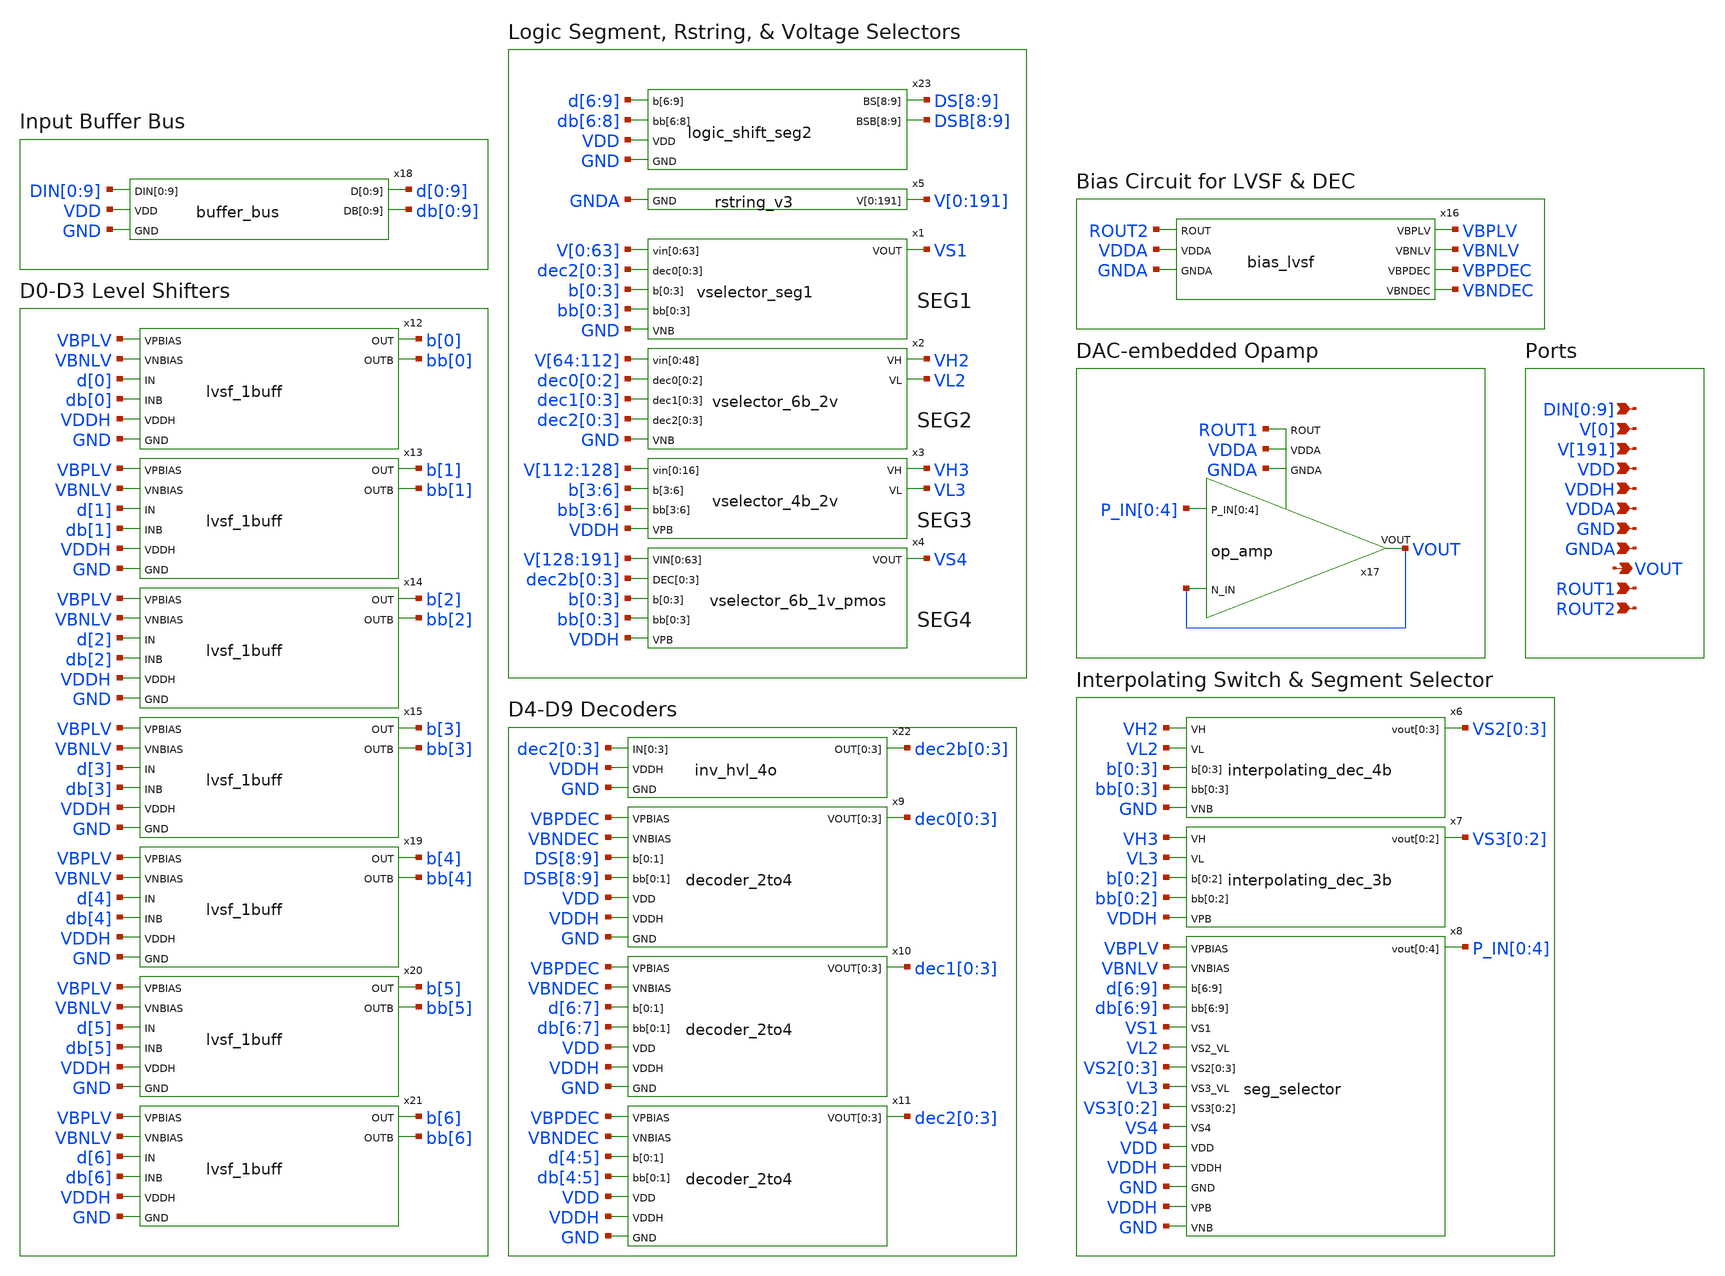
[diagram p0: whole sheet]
** sch_path: xschem/10b_DAC_top.sch
**.subckt 10b_DAC_top VOUT GND DIN[0],DIN[1],DIN[2],DIN[3],DIN[4],DIN[5],DIN[6],DIN[7],DIN[8],DIN[9]
*+ VDD VDDH VDDA GNDA ROUT1 ROUT2 V[0] V[191]
*.opin VOUT
*.ipin GND
*.ipin DIN[0],DIN[1],DIN[2],DIN[3],DIN[4],DIN[5],DIN[6],DIN[7],DIN[8],DIN[9]
*.ipin VDD
*.ipin VDDH
*.ipin VDDA
*.ipin GNDA
*.ipin ROUT1
*.ipin ROUT2
*.ipin V[0]
*.ipin V[191]
x2 V[64] V[65] V[66] V[67] V[68] V[69] V[70] V[71] V[72] V[73] V[74] V[75] V[76] V[77] V[78] V[79]
+ V[80] V[81] V[82] V[83] V[84] V[85] V[86] V[87] V[88] V[89] V[90] V[91] V[92] V[93] V[94] V[95] V[96]
+ V[97] V[98] V[99] V[100] V[101] V[102] V[103] V[104] V[105] V[106] V[107] V[108] V[109] V[110] V[111]
+ V[112] dec0[0] dec0[1] dec0[2] dec1[0] dec1[1] dec1[2] dec1[3] dec2[0] dec2[1] dec2[2] dec2[3] VH2 VL2 GND
+ vselector_6b_2v
x3 V[112] V[113] V[114] V[115] V[116] V[117] V[118] V[119] V[120] V[121] V[122] V[123] V[124] V[125]
+ V[126] V[127] V[128] b[3] b[4] b[5] b[6] bb[3] bb[4] bb[5] bb[6] VH3 VL3 VDDH vselector_4b_2v
x4 V[128] V[129] V[130] V[131] V[132] V[133] V[134] V[135] V[136] V[137] V[138] V[139] V[140] V[141]
+ V[142] V[143] V[144] V[145] V[146] V[147] V[148] V[149] V[150] V[151] V[152] V[153] V[154] V[155] V[156]
+ V[157] V[158] V[159] V[160] V[161] V[162] V[163] V[164] V[165] V[166] V[167] V[168] V[169] V[170] V[171]
+ V[172] V[173] V[174] V[175] V[176] V[177] V[178] V[179] V[180] V[181] V[182] V[183] V[184] V[185] V[186]
+ V[187] V[188] V[189] V[190] V[191] dec2b[0] dec2b[1] dec2b[2] dec2b[3] b[0] b[1] b[2] b[3] bb[0] bb[1]
+ bb[2] bb[3] VS4 VDDH vselector_6b_1v_pmos
x6 VH2 VL2 b[0] b[1] b[2] b[3] bb[0] bb[1] bb[2] bb[3] VS2[0] VS2[1] VS2[2] VS2[3] GND
+ interpolating_dec_4b
x7 VH3 VL3 b[0] b[1] b[2] bb[0] bb[1] bb[2] VS3[0] VS3[1] VS3[2] VDDH interpolating_dec_3b
x8 VBPLV VBNLV d[6] d[7] d[8] d[9] db[6] db[7] db[8] db[9] VS1 VL2 VS2[0] VS2[1] VS2[2] VS2[3] VL3
+ VS3[0] VS3[1] VS3[2] VS4 P_IN[0] P_IN[1] P_IN[2] P_IN[3] P_IN[4] VDD VDDH GND VDDH GND seg_selector
x9 VBPDEC VBNDEC DS[8] DS[9] DSB[8] DSB[9] dec0[0] dec0[1] dec0[2] dec0[3] VDD VDDH GND decoder_2to4
x10 VBPDEC VBNDEC d[6] d[7] db[6] db[7] dec1[0] dec1[1] dec1[2] dec1[3] VDD VDDH GND decoder_2to4
x11 VBPDEC VBNDEC d[4] d[5] db[4] db[5] dec2[0] dec2[1] dec2[2] dec2[3] VDD VDDH GND decoder_2to4
x1 V[0] V[1] V[2] V[3] V[4] V[5] V[6] V[7] V[8] V[9] V[10] V[11] V[12] V[13] V[14] V[15] V[16] V[17]
+ V[18] V[19] V[20] V[21] V[22] V[23] V[24] V[25] V[26] V[27] V[28] V[29] V[30] V[31] V[32] V[33] V[34]
+ V[35] V[36] V[37] V[38] V[39] V[40] V[41] V[42] V[43] V[44] V[45] V[46] V[47] V[48] V[49] V[50] V[51]
+ V[52] V[53] V[54] V[55] V[56] V[57] V[58] V[59] V[60] V[61] V[62] V[63] dec2[0] dec2[1] dec2[2] dec2[3]
+ b[0] b[1] b[2] b[3] bb[0] bb[1] bb[2] bb[3] VS1 GND vselector_seg1
x12 VBPLV VBNLV d[0] db[0] b[0] bb[0] VDDH GND lvsf_1buff
x13 VBPLV VBNLV d[1] db[1] b[1] bb[1] VDDH GND lvsf_1buff
x14 VBPLV VBNLV d[2] db[2] b[2] bb[2] VDDH GND lvsf_1buff
x15 VBPLV VBNLV d[3] db[3] b[3] bb[3] VDDH GND lvsf_1buff
x17 P_IN[0] P_IN[1] P_IN[2] P_IN[3] P_IN[4] VOUT VOUT ROUT1 VDDA GNDA op_amp
x16 ROUT2 VBPLV VBNLV VBPDEC VBNDEC VDDA GNDA bias_lvsf
x18 DIN[0] DIN[1] DIN[2] DIN[3] DIN[4] DIN[5] DIN[6] DIN[7] DIN[8] DIN[9] d[0] d[1] d[2] d[3] d[4]
+ d[5] d[6] d[7] d[8] d[9] db[0] db[1] db[2] db[3] db[4] db[5] db[6] db[7] db[8] db[9] VDD GND buffer_bus
x19 VBPLV VBNLV d[4] db[4] b[4] bb[4] VDDH GND lvsf_1buff
x20 VBPLV VBNLV d[5] db[5] b[5] bb[5] VDDH GND lvsf_1buff
x21 VBPLV VBNLV d[6] db[6] b[6] bb[6] VDDH GND lvsf_1buff
x22 dec2[0] dec2[1] dec2[2] dec2[3] dec2b[0] dec2b[1] dec2b[2] dec2b[3] VDDH GND inv_hvl_4o
x23 d[6] d[7] d[8] d[9] db[6] db[7] db[8] DS[8] DS[9] DSB[8] DSB[9] VDD GND logic_shift_seg2
x5 V[0] V[1] V[2] V[3] V[4] V[5] V[6] V[7] V[8] V[9] V[10] V[11] V[12] V[13] V[14] V[15] V[16] V[17]
+ V[18] V[19] V[20] V[21] V[22] V[23] V[24] V[25] V[26] V[27] V[28] V[29] V[30] V[31] V[32] V[33] V[34]
+ V[35] V[36] V[37] V[38] V[39] V[40] V[41] V[42] V[43] V[44] V[45] V[46] V[47] V[48] V[49] V[50] V[51]
+ V[52] V[53] V[54] V[55] V[56] V[57] V[58] V[59] V[60] V[61] V[62] V[63] V[64] V[65] V[66] V[67] V[68]
+ V[69] V[70] V[71] V[72] V[73] V[74] V[75] V[76] V[77] V[78] V[79] V[80] V[81] V[82] V[83] V[84] V[85]
+ V[86] V[87] V[88] V[89] V[90] V[91] V[92] V[93] V[94] V[95] V[96] V[97] V[98] V[99] V[100] V[101] V[102]
+ V[103] V[104] V[105] V[106] V[107] V[108] V[109] V[110] V[111] V[112] V[113] V[114] V[115] V[116] V[117]
+ V[118] V[119] V[120] V[121] V[122] V[123] V[124] V[125] V[126] V[127] V[128] V[129] V[130] V[131] V[132]
+ V[133] V[134] V[135] V[136] V[137] V[138] V[139] V[140] V[141] V[142] V[143] V[144] V[145] V[146] V[147]
+ V[148] V[149] V[150] V[151] V[152] V[153] V[154] V[155] V[156] V[157] V[158] V[159] V[160] V[161] V[162]
+ V[163] V[164] V[165] V[166] V[167] V[168] V[169] V[170] V[171] V[172] V[173] V[174] V[175] V[176] V[177]
+ V[178] V[179] V[180] V[181] V[182] V[183] V[184] V[185] V[186] V[187] V[188] V[189] V[190] V[191] GNDA
+ rstring_v3
**.ends
.end
